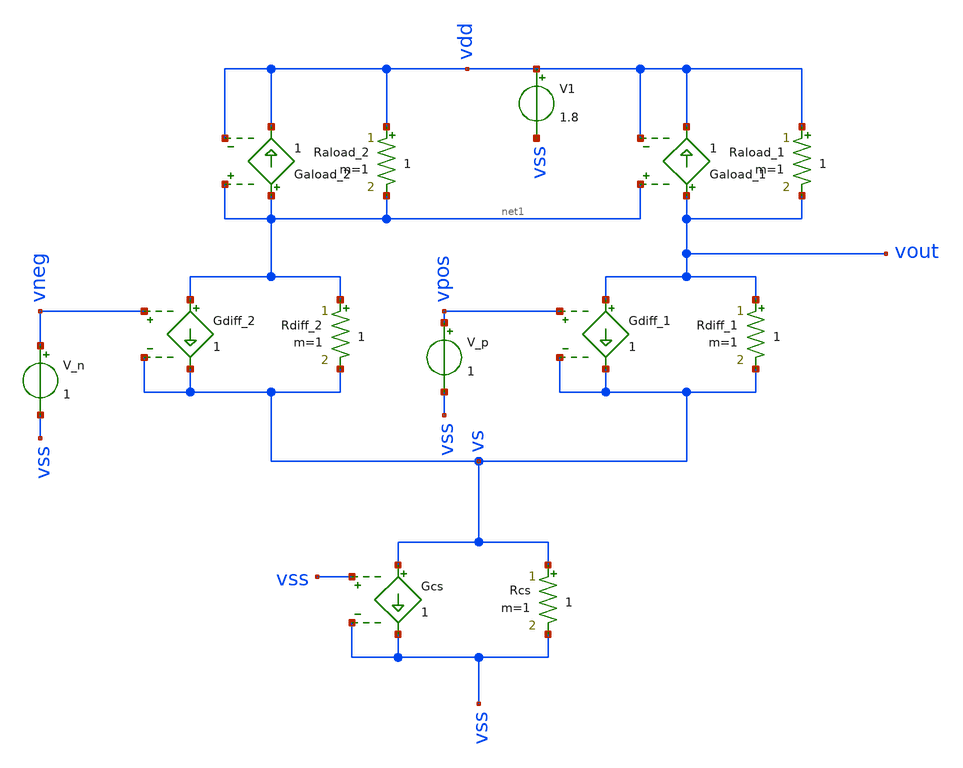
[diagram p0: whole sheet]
** sch_path: test/Tesis_notebooks/xschem/ota_1stage.sch
**.subckt ota_1stage
Rdiff_2 net1 vs 1 m=1
Gdiff_2 net1 vs vneg vs 1
Rdiff_1 vout vs 1 m=1
Gdiff_1 vout vs vpos vs 1
V1 vdd vss 1.8
V_n vneg vss 1
V_p vpos vss 1
Raload_1 vdd vout 1 m=1
Gaload_1 vout vdd net1 vdd 1
Gaload_2 net1 vdd net1 vdd 1
Raload_2 vdd net1 1 m=1
Rcs vs vss 1 m=1
Gcs vs vss vss vss 1
**.ends
.end
